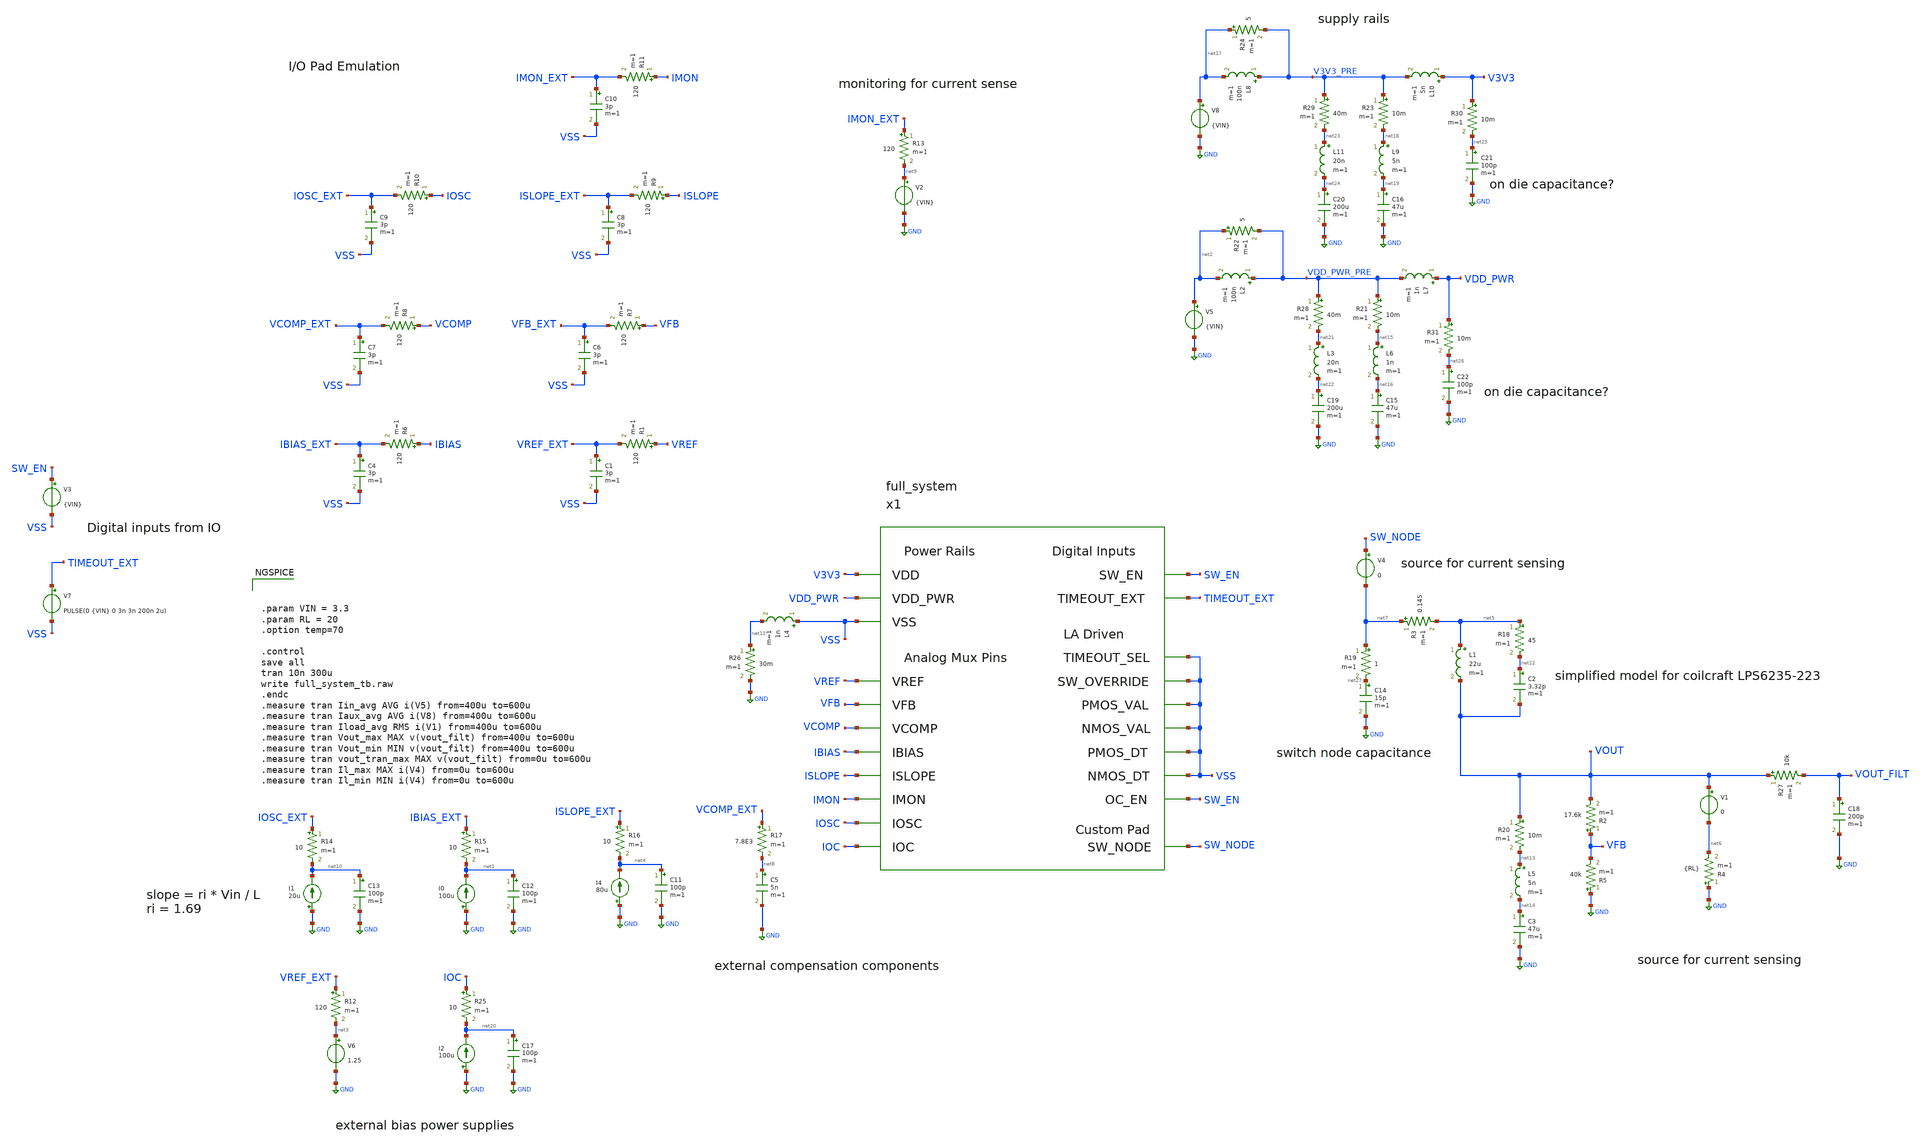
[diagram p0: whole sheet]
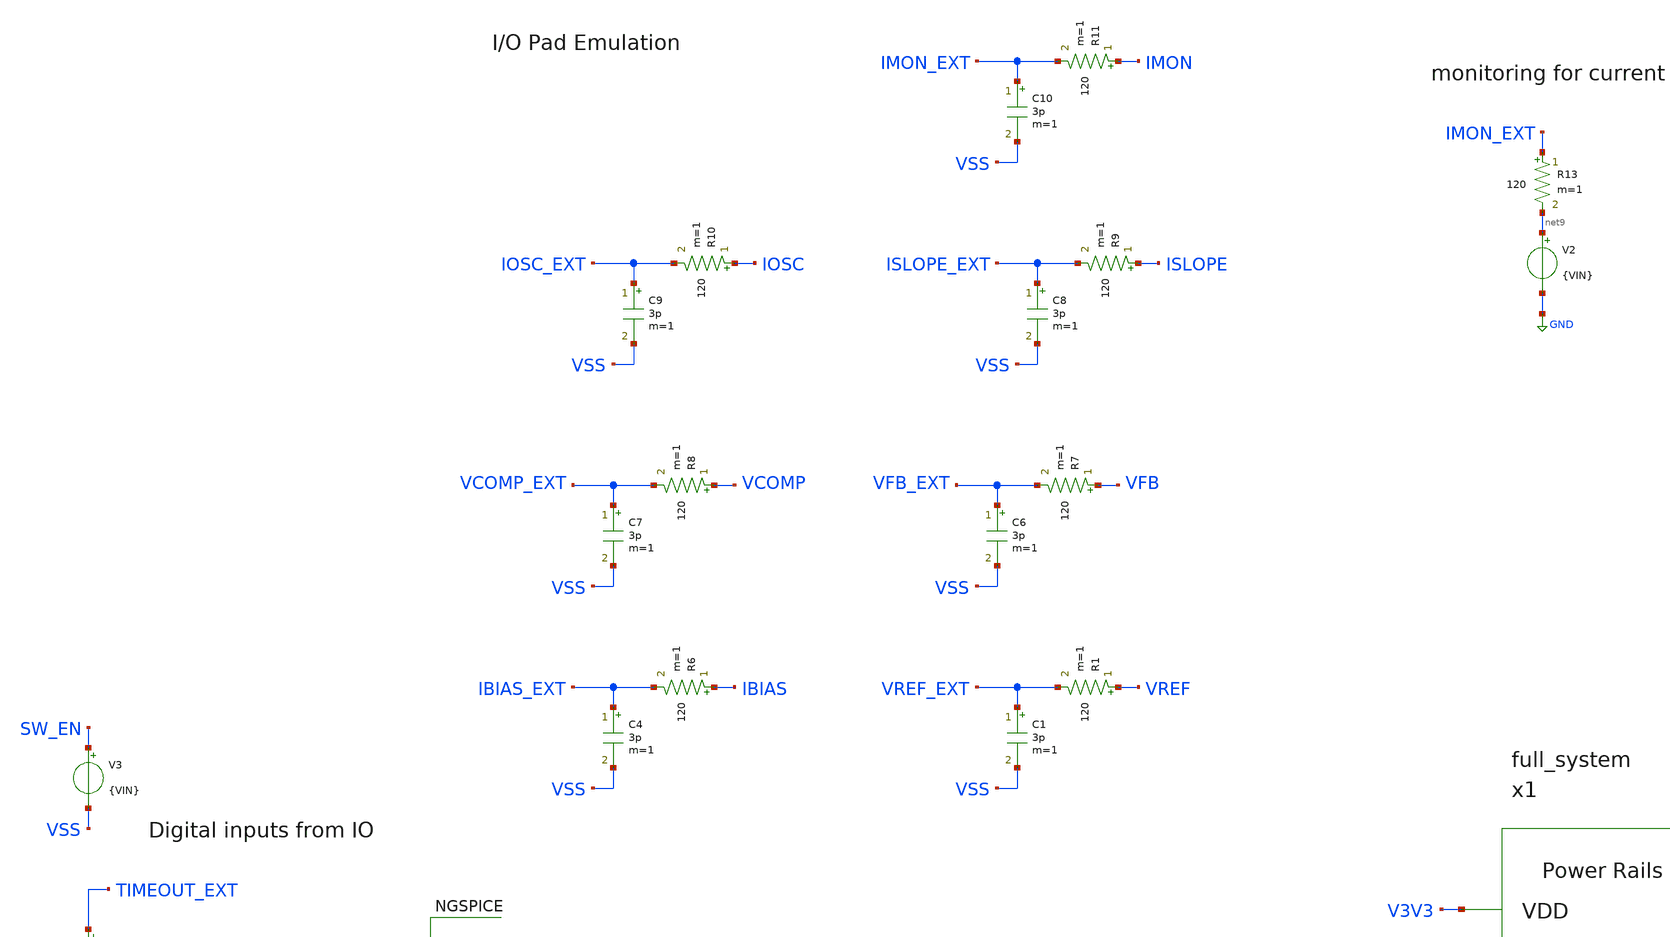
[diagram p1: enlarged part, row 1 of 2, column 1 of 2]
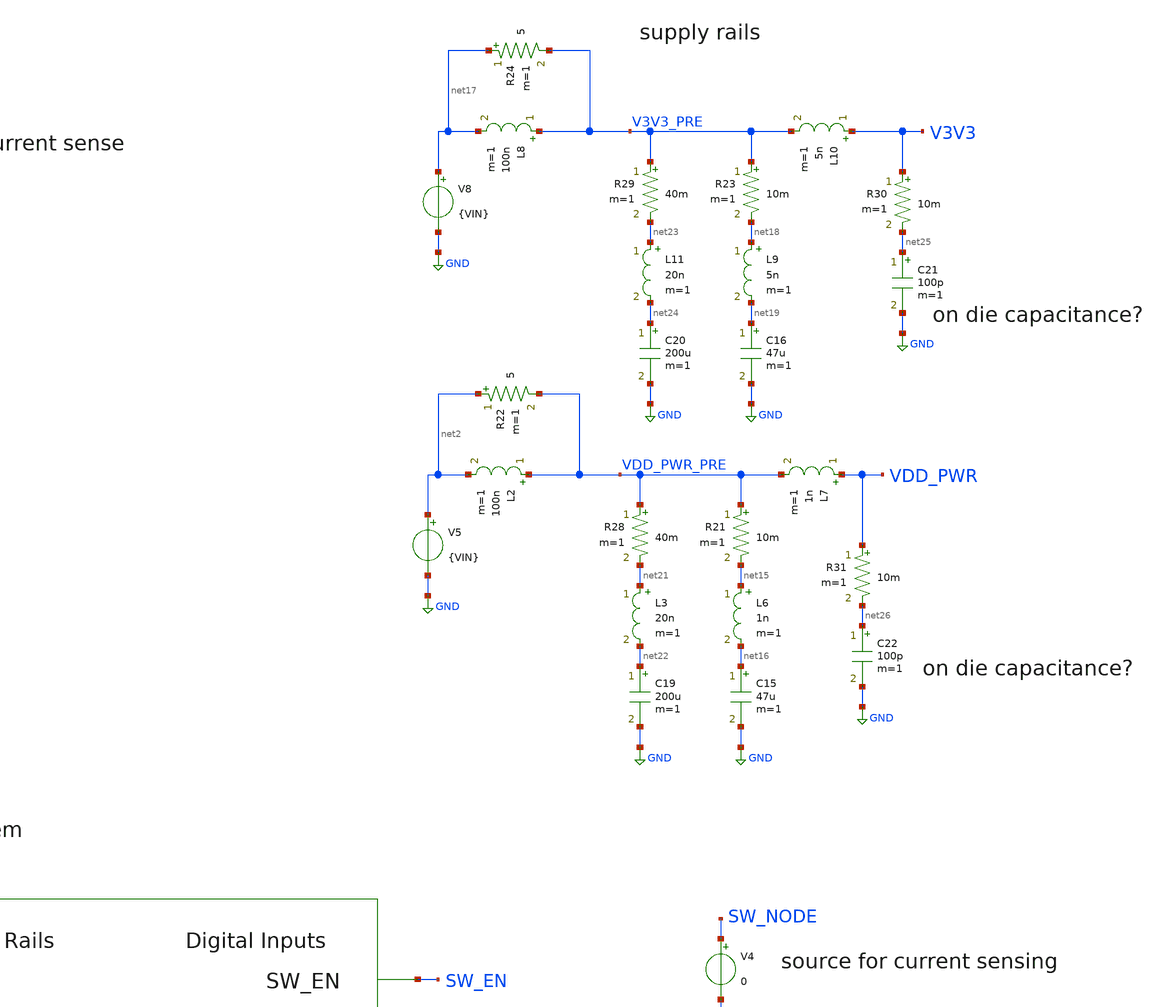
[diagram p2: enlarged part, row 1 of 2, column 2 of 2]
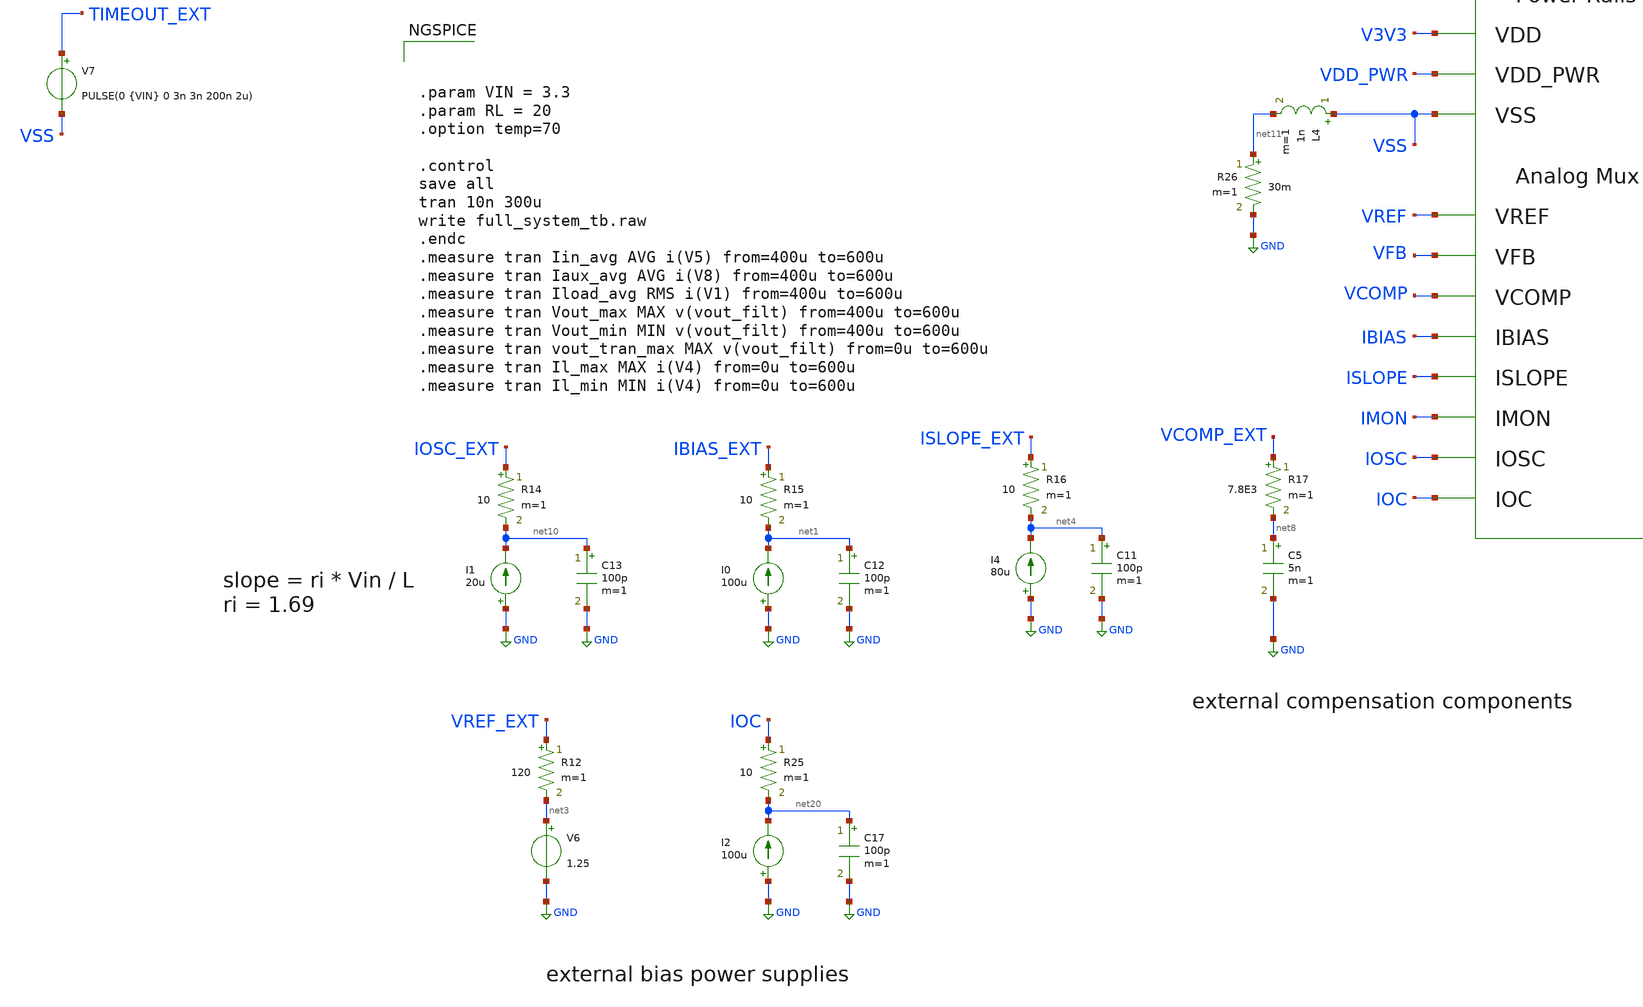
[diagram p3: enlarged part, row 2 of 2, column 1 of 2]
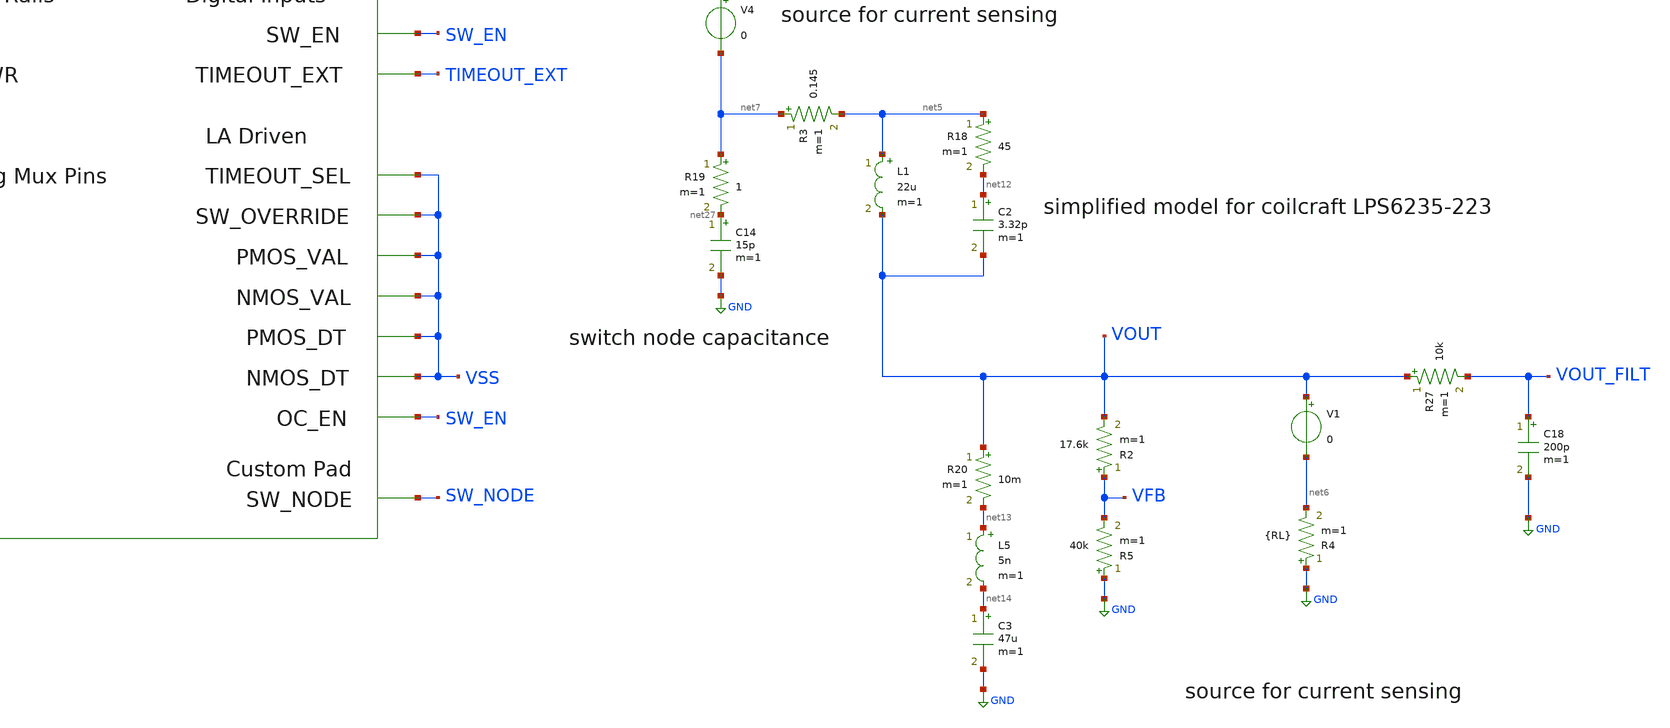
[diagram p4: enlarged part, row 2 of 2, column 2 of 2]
** sch_path: images/foss-asic-tools/addons/examples/open-pmic/design/system/full_system_tb.sch
**.subckt full_system_tb
I0 GND net1 100u
V5 net2 GND {VIN}
V6 net3 GND 1.25
I4 GND net4 80u
x1 V3V3 VDD_PWR VSS VREF VFB VCOMP IBIAS ISLOPE IMON IOSC SW_EN TIMEOUT_EXT VSS VSS VSS VSS VSS VSS
+ SW_NODE IOC SW_EN full_system
L1 net5 VOUT 22u m=1
R3 net7 net5 0.145 m=1
C2 net12 VOUT 3.32p m=1
C3 net14 GND 47u m=1
R4 GND net6 {RL} m=1
V4 SW_NODE net7 0
R2 VFB VOUT 17.6k m=1
R5 GND VFB 40k m=1
C5 net8 GND 5n m=1
V2 net9 GND {VIN}
I1 GND net10 20u
V7 TIMEOUT_EXT VSS PULSE(0 {VIN} 0 3n 3n 200n 2u)
V3 SW_EN VSS {VIN}
R1 VREF VREF_EXT 120 m=1
C1 VREF_EXT VSS 3p m=1
R6 IBIAS IBIAS_EXT 120 m=1
C4 IBIAS_EXT VSS 3p m=1
R7 VFB VFB_EXT 120 m=1
C6 VFB_EXT VSS 3p m=1
R8 VCOMP VCOMP_EXT 120 m=1
C7 VCOMP_EXT VSS 3p m=1
R9 ISLOPE ISLOPE_EXT 120 m=1
C8 ISLOPE_EXT VSS 3p m=1
R10 IOSC IOSC_EXT 120 m=1
C9 IOSC_EXT VSS 3p m=1
R11 IMON IMON_EXT 120 m=1
C10 IMON_EXT VSS 3p m=1
R12 VREF_EXT net3 120 m=1
R13 IMON_EXT net9 120 m=1
R14 IOSC_EXT net10 10 m=1
R15 IBIAS_EXT net1 10 m=1
R16 ISLOPE_EXT net4 10 m=1
R17 VCOMP_EXT net8 7.8E3 m=1
L2 VDD_PWR_PRE net2 100n m=1
L4 VSS net11 1n m=1
C11 net4 GND 100p m=1
C12 net1 GND 100p m=1
C13 net10 GND 100p m=1
R18 net5 net12 45 m=1
C14 net27 GND 15p m=1
R19 net7 net27 1 m=1
L5 net13 net14 5n m=1
R20 VOUT net13 10m m=1
C15 net16 GND 47u m=1
L6 net15 net16 1n m=1
R21 VDD_PWR_PRE net15 10m m=1
L7 VDD_PWR VDD_PWR_PRE 1n m=1
R22 net2 VDD_PWR_PRE 5 m=1
V8 net17 GND {VIN}
L8 V3V3_PRE net17 100n m=1
C16 net19 GND 47u m=1
L9 net18 net19 5n m=1
R23 V3V3_PRE net18 10m m=1
L10 V3V3 V3V3_PRE 5n m=1
R24 net17 V3V3_PRE 5 m=1
V1 VOUT net6 0
I2 GND net20 100u
R25 IOC net20 10 m=1
C17 net20 GND 100p m=1
R26 net11 GND 30m m=1
R27 VOUT VOUT_FILT 10k m=1
C18 VOUT_FILT GND 200p m=1
C19 net22 GND 200u m=1
L3 net21 net22 20n m=1
R28 VDD_PWR_PRE net21 40m m=1
C20 net24 GND 200u m=1
L11 net23 net24 20n m=1
R29 V3V3_PRE net23 40m m=1
C21 net25 GND 100p m=1
R30 V3V3 net25 10m m=1
C22 net26 GND 100p m=1
R31 VDD_PWR net26 10m m=1
**** begin user architecture code



.param VIN = 3.3
.param RL = 20
.option temp=70

.control
save all
tran 10n 300u
write full_system_tb.raw
.endc
.measure tran Iin_avg AVG i(V5) from=400u to=600u
.measure tran Iaux_avg AVG i(V8) from=400u to=600u
.measure tran Iload_avg RMS i(V1) from=400u to=600u
.measure tran Vout_max MAX v(vout_filt) from=400u to=600u
.measure tran Vout_min MIN v(vout_filt) from=400u to=600u
.measure tran vout_tran_max MAX v(vout_filt) from=0u to=600u
.measure tran Il_max MAX i(V4) from=0u to=600u
.measure tran Il_min MIN i(V4) from=0u to=600u



.lib $::SKYWATER_MODELS/models/sky130.lib.spice ss
.option wnflag=1

**** end user architecture code
**.ends
.GLOBAL GND
**** begin user architecture code
[sky130_models]
**** end user architecture code
.end
